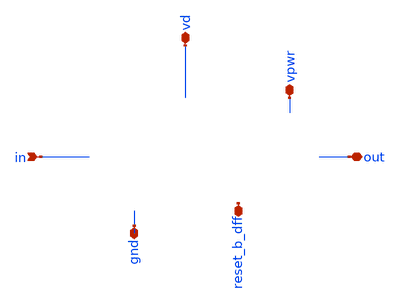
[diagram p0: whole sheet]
** sch_path: mag/sigma-delta_modulator/xschem/sigma-delta-pex.sch
* Copyright 2020 Stefan Frederik Schippers
* Licensed under the Apache License, Version 2.0 (the "License");
* you may not use this file except in compliance with the License.
* You may obtain a copy of the License at
* https://www.apache.org/licenses/LICENSE-2.0
* Unless required by applicable law or agreed to in writing, software
* distributed under the License is distributed on an "AS IS" BASIS,
* WITHOUT WARRANTIES OR CONDITIONS OF ANY KIND, either express or implied.
* See the License for the specific language governing permissions and
* limitations under the License.
**.subckt sigma-delta-pex in gnd out reset_b_dff vpwr vd
*.ipin in
*.iopin gnd
*.iopin out
*.iopin reset_b_dff
*.iopin vpwr
*.iopin vd
**** begin user architecture code



* NGSPICE file created from sigma-delta.ext - technology: sky130A

*.subckt sigma-delta reset_b_dff gnd vd in clk vpwr out
X0 a_n1599_309# a_n1774_335# a_n1420_335# gnd.t20 sky130_fd_pr__nfet_01v8 ad=0.109 pd=1.36 as=0.064
+ ps=0.725 w=0.42 l=0.15
X1 a_n2266_4800# a_n2100_3468# gnd.t7 sky130_fd_pr__res_xhigh_po_0p35 l=4.5
X2 a_n1124_4800# a_n958_3468# gnd.t50 sky130_fd_pr__res_xhigh_po_0p35 l=4.5
X3 x1.Q a_n1599_309# vpwr.t5 vpwr.t4 sky130_fd_pr__pfet_01v8_hvt ad=0.28 pd=2.56 as=0.213 ps=1.67
+ w=1 l=0.15
X4 a_n2339_335# a_n2689_335# a_n2434_335# vpwr.t15 sky130_fd_pr__pfet_01v8_hvt ad=0.0724 pd=0.765
+ as=0.0651 ps=0.73 w=0.42 l=0.15
X5 a_n2121_577# a_n2339_335# vpwr.t21 vpwr.t20 sky130_fd_pr__pfet_01v8_hvt ad=0.129 pd=1.18 as=0.218
+ ps=2.2 w=0.84 l=0.15
X6 a_n1420_335# reset_b_dff.t0 gnd.t52 gnd.t51 sky130_fd_pr__nfet_01v8 ad=0.064 pd=0.725 as=0.125
+ ps=1.01 w=0.42 l=0.15
X7 a_n792_4800# a_n626_3468# gnd.t8 sky130_fd_pr__res_xhigh_po_0p35 l=4.5
X8 a_n2714_2632# a_n2880_1800# gnd.t10 sky130_fd_pr__res_xhigh_po_0p35 l=2
X9 out.t0 a_n1035_335# gnd.t19 gnd.t18 sky130_fd_pr__nfet_01v8 ad=0.169 pd=1.82 as=0.1 ps=0.985
+ w=0.65 l=0.15
X10 a_n1934_4800# a_n2100_3468# gnd.t27 sky130_fd_pr__res_xhigh_po_0p35 l=4.5
X11 in_comp a_n1884_1800# gnd.t26 sky130_fd_pr__res_xhigh_po_0p35 l=2
X12 a_n1612_701# a_n2689_335# a_n1774_335# vpwr.t14 sky130_fd_pr__pfet_01v8_hvt ad=0.0567 pd=0.69
+ as=0.0588 ps=0.7 w=0.42 l=0.15
X13 a_n2077_335# a_n2121_577# a_n2243_335# gnd.t41 sky130_fd_pr__nfet_01v8 ad=0.0441 pd=0.63 as=0.14
+ ps=1.1 w=0.42 l=0.15
X14 a_n2434_335# x1.D gnd.t44 gnd.t43 sky130_fd_pr__nfet_01v8 ad=0.066 pd=0.745 as=0.221 ps=1.89
+ w=0.42 l=0.15
X15 a_n1599_309# reset_b_dff.t1 vpwr.t11 vpwr.t10 sky130_fd_pr__pfet_01v8_hvt ad=0.0567 pd=0.69
+ as=0.0819 ps=0.81 w=0.42 l=0.15
X16 a_n2598_4800# a_n2764_3468# gnd.t25 sky130_fd_pr__res_xhigh_po_0p35 l=4.5
X17 a_n1665_335# a_n2855_335# a_n1774_335# gnd.t38 sky130_fd_pr__nfet_01v8 ad=0.0669 pd=0.75
+ as=0.0711 ps=0.755 w=0.36 l=0.15
X18 a_n1456_4800# in_int gnd.t32 sky130_fd_pr__res_xhigh_po_0p35 l=4.5
X19 gnd.t6 a_n1599_309# a_n1665_335# gnd.t5 sky130_fd_pr__nfet_01v8 ad=0.125 pd=1.01 as=0.0669
+ ps=0.75 w=0.42 l=0.15
X20 a_n2434_335# x1.D vpwr.t25 vpwr.t24 sky130_fd_pr__pfet_01v8_hvt ad=0.0651 pd=0.73 as=0.109
+ ps=1.36 w=0.42 l=0.15
X21 vpwr.t3 a_n1599_309# a_n1612_701# vpwr.t2 sky130_fd_pr__pfet_01v8_hvt ad=0.0819 pd=0.81
+ as=0.0567 ps=0.69 w=0.42 l=0.15
X22 vpwr.t9 a_n1774_335# a_n1599_309# vpwr.t8 sky130_fd_pr__pfet_01v8_hvt ad=0.213 pd=1.67 as=0.0567
+ ps=0.69 w=0.42 l=0.15
X23 a_n2121_577# a_n2339_335# gnd.t40 gnd.t39 sky130_fd_pr__nfet_01v8 ad=0.0999 pd=0.985 as=0.135
+ ps=1.15 w=0.64 l=0.15
X24 vpwr.t27 clk.t0 a_n2855_335# vpwr.t26 sky130_fd_pr__pfet_01v8_hvt ad=0.0864 pd=0.91 as=0.166
+ ps=1.8 w=0.64 l=0.15
X25 gnd.t15 reset_b_dff.t2 a_n2077_335# gnd.t14 sky130_fd_pr__nfet_01v8 ad=0.135 pd=1.15 as=0.0441
+ ps=0.63 w=0.42 l=0.15
X26 vpwr.t1 a_n1599_309# a_n1035_335# vpwr.t0 sky130_fd_pr__pfet_01v8_hvt ad=0.154 pd=1.34 as=0.166
+ ps=1.8 w=0.64 l=0.15
X27 gnd.t4 a_n1599_309# a_n1035_335# gnd.t3 sky130_fd_pr__nfet_01v8 ad=0.1 pd=0.985 as=0.109 ps=1.36
+ w=0.42 l=0.15
X28 a_n2266_4800# a_n2432_3468# gnd.t17 sky130_fd_pr__res_xhigh_po_0p35 l=4.5
X29 a_n2050_2632# a_n2216_1800# gnd.t11 sky130_fd_pr__res_xhigh_po_0p35 l=2
X30 gnd.t22 clk.t1 a_n2855_335# gnd.t21 sky130_fd_pr__nfet_01v8 ad=0.0567 pd=0.69 as=0.109 ps=1.36
+ w=0.42 l=0.15
X31 a_n2243_335# a_n2689_335# a_n2339_335# gnd.t34 sky130_fd_pr__nfet_01v8 ad=0.14 pd=1.1 as=0.0594
+ ps=0.69 w=0.36 l=0.15
X32 vd.t1 in_comp x1.D vd.t0 sky130_fd_pr__pfet_01v8 ad=0.87 pd=6.58 as=0.87 ps=6.58 w=3 l=0.15
X33 a_n1124_4800# a_n1290_3468# gnd.t45 sky130_fd_pr__res_xhigh_po_0p35 l=4.5
X34 a_n2339_335# a_n2855_335# a_n2434_335# gnd.t37 sky130_fd_pr__nfet_01v8 ad=0.0594 pd=0.69
+ as=0.066 ps=0.745 w=0.36 l=0.15
X35 a_n460_4800# x1.Q gnd.t53 sky130_fd_pr__res_xhigh_po_0p35 l=4.5
X36 a_n2689_335# a_n2855_335# vpwr.t19 vpwr.t18 sky130_fd_pr__pfet_01v8_hvt ad=0.166 pd=1.8
+ as=0.0864 ps=0.91 w=0.64 l=0.15
X37 a_n2231_701# a_n2855_335# a_n2339_335# vpwr.t17 sky130_fd_pr__pfet_01v8_hvt ad=0.116 pd=0.97
+ as=0.0724 ps=0.765 w=0.42 l=0.15
X38 a_n2689_335# a_n2855_335# gnd.t36 gnd.t35 sky130_fd_pr__nfet_01v8 ad=0.109 pd=1.36 as=0.0567
+ ps=0.69 w=0.42 l=0.15
X39 a_n1774_335# a_n2855_335# a_n2121_577# vpwr.t16 sky130_fd_pr__pfet_01v8_hvt ad=0.0588 pd=0.7
+ as=0.129 ps=1.18 w=0.42 l=0.15
X40 a_n2382_2632# a_n2548_1800# gnd.t31 sky130_fd_pr__res_xhigh_po_0p35 l=2
X41 in_int a_n2880_1800# gnd.t16 sky130_fd_pr__res_xhigh_po_0p35 l=2
X42 x1.Q a_n1599_309# gnd.t2 gnd.t1 sky130_fd_pr__nfet_01v8 ad=0.169 pd=1.82 as=0.169 ps=1.82 w=0.65
+ l=0.15
X43 in_comp gnd.t30 sky130_fd_pr__cap_mim_m3_1 l=27.2 w=27.2
X44 a_n460_4800# a_n626_3468# gnd.t13 sky130_fd_pr__res_xhigh_po_0p35 l=4.5
X45 a_n2231_701# reset_b_dff.t3 vpwr.t13 vpwr.t12 sky130_fd_pr__pfet_01v8_hvt ad=0.109 pd=1.36
+ as=0.0703 ps=0.755 w=0.42 l=0.15
X46 a_n2930_4800# a_n2764_3468# gnd.t12 sky130_fd_pr__res_xhigh_po_0p35 l=4.5
X47 in_int gnd.t42 sky130_fd_pr__cap_mim_m3_1 l=27.2 w=27.2
X48 a_n2714_2632# a_n2548_1800# gnd.t24 sky130_fd_pr__res_xhigh_po_0p35 l=2
X49 gnd.t29 in_comp x1.D gnd.t28 sky130_fd_pr__nfet_01v8 ad=0.29 pd=2.58 as=0.29 ps=2.58 w=1 l=0.15
X50 a_n1934_4800# in_int gnd.t46 sky130_fd_pr__res_xhigh_po_0p35 l=4.5
X51 a_n792_4800# a_n958_3468# gnd.t9 sky130_fd_pr__res_xhigh_po_0p35 l=4.5
X52 vpwr.t23 a_n2121_577# a_n2231_701# vpwr.t22 sky130_fd_pr__pfet_01v8_hvt ad=0.0703 pd=0.755
+ as=0.116 ps=0.97 w=0.42 l=0.15
X53 a_n1774_335# a_n2689_335# a_n2121_577# gnd.t33 sky130_fd_pr__nfet_01v8 ad=0.0711 pd=0.755
+ as=0.0999 ps=0.985 w=0.36 l=0.15
X54 a_n2598_4800# a_n2432_3468# gnd.t49 sky130_fd_pr__res_xhigh_po_0p35 l=4.5
X55 a_n2382_2632# a_n2216_1800# gnd.t48 sky130_fd_pr__res_xhigh_po_0p35 l=2
X56 a_n2930_4800# in.t0 gnd.t23 sky130_fd_pr__res_xhigh_po_0p35 l=4.5
X57 a_n1456_4800# a_n1290_3468# gnd.t0 sky130_fd_pr__res_xhigh_po_0p35 l=4.5
X58 a_n2050_2632# a_n1884_1800# gnd.t47 sky130_fd_pr__res_xhigh_po_0p35 l=2
X59 out.t1 a_n1035_335# vpwr.t7 vpwr.t6 sky130_fd_pr__pfet_01v8_hvt ad=0.26 pd=2.52 as=0.154 ps=1.34
+ w=1 l=0.15
R0 gnd.n76 gnd.n12 1509.66
R1 gnd.n9 gnd.n3 1273.6
R2 gnd.n10 gnd.n9 1263.33
R3 gnd.t18 gnd.n84 1127.78
R4 gnd.t35 gnd.t43 1049.58
R5 gnd.n84 gnd.n83 788.875
R6 gnd.t1 gnd.t3 773.808
R7 gnd.t20 gnd.t1 773.808
R8 gnd.t34 gnd.t41 683.255
R9 gnd.t5 gnd.t51 613.284
R10 gnd.t14 gnd.t39 543.312
R11 gnd.t33 gnd.t38 448.644
R12 gnd.t39 gnd.t33 407.485
R13 gnd.t3 gnd.t18 399.252
R14 gnd.t38 gnd.t5 395.137
R15 gnd.t37 gnd.t34 395.137
R16 gnd.t43 gnd.t37 391.021
R17 gnd.t51 gnd.t20 374.557
R18 gnd.t21 gnd.t35 345.745
R19 gnd.t41 gnd.t14 296.353
R20 gnd gnd.t21 267.541
R21 gnd.n12 gnd.t53 238.407
R22 gnd.n23 gnd.t44 215.036
R23 gnd.n2 gnd.t23 190.731
R24 gnd.t53 gnd.t13 184.073
R25 gnd.t13 gnd.t8 184.073
R26 gnd.t8 gnd.t9 184.073
R27 gnd.t9 gnd.t50 184.073
R28 gnd.t50 gnd.t45 184.073
R29 gnd.t45 gnd.t0 184.073
R30 gnd.n7 gnd.t26 176.31
R31 gnd.n32 gnd.t2 154.317
R32 gnd.n81 gnd.n1 149.835
R33 gnd.n81 gnd.n80 149.835
R34 gnd.n34 gnd.n33 128.757
R35 gnd.t27 gnd.t11 128.63
R36 gnd.t7 gnd.t48 128.63
R37 gnd.t17 gnd.t31 128.63
R38 gnd.t49 gnd.t24 128.63
R39 gnd.t25 gnd.t10 128.63
R40 gnd.t12 gnd.t16 128.63
R41 gnd.n30 gnd.n29 116.754
R42 gnd.n7 gnd.t32 114.215
R43 gnd.n62 gnd.n21 107.24
R44 gnd.n49 gnd.n48 107.24
R45 gnd.n29 gnd.t52 100.001
R46 gnd.t46 gnd.n4 99.7989
R47 gnd.n80 gnd.n78 98.6358
R48 gnd.n48 gnd.t15 72.8576
R49 gnd.n29 gnd.t6 70.0005
R50 gnd.n48 gnd.t40 60.5809
R51 gnd.n33 gnd.t4 57.1434
R52 gnd.t26 gnd.t46 55.444
R53 gnd.t47 gnd.t27 55.444
R54 gnd.t11 gnd.t7 55.444
R55 gnd.t48 gnd.t17 55.444
R56 gnd.t31 gnd.t49 55.444
R57 gnd.t24 gnd.t25 55.444
R58 gnd.t10 gnd.t12 55.444
R59 gnd.n21 gnd.t36 38.5719
R60 gnd.n21 gnd.t22 38.5719
R61 gnd.n37 gnd.n36 34.6358
R62 gnd.n38 gnd.n37 34.6358
R63 gnd.n42 gnd.n41 34.6358
R64 gnd.n43 gnd.n42 34.6358
R65 gnd.n43 gnd.n27 34.6358
R66 gnd.n47 gnd.n27 34.6358
R67 gnd.n51 gnd.n50 34.6358
R68 gnd.n51 gnd.n25 34.6358
R69 gnd.n55 gnd.n25 34.6358
R70 gnd.n56 gnd.n55 34.6358
R71 gnd.n57 gnd.n56 34.6358
R72 gnd.n61 gnd.n23 29.7417
R73 gnd.n4 gnd.t47 28.8311
R74 gnd.n36 gnd.n32 27.8593
R75 gnd.n12 gnd.n11 26.7279
R76 gnd.n33 gnd.t19 25.4291
R77 gnd.n63 gnd.n62 24.4919
R78 gnd.n62 gnd.n61 22.9652
R79 gnd.n38 gnd.n30 17.6946
R80 gnd.n16 gnd.t29 17.405
R81 gnd.n57 gnd.n23 14.6829
R82 gnd.n34 gnd.n32 10.9075
R83 gnd.n16 gnd.n15 9.33321
R84 gnd.n50 gnd.n49 7.90638
R85 gnd.n50 gnd.n26 4.6505
R86 gnd.n59 gnd.n23 4.6505
R87 gnd.n62 gnd.n22 4.6505
R88 gnd.n52 gnd.n51 4.6505
R89 gnd.n53 gnd.n25 4.6505
R90 gnd.n55 gnd.n54 4.6505
R91 gnd.n56 gnd.n24 4.6505
R92 gnd.n58 gnd.n57 4.6505
R93 gnd.n61 gnd.n60 4.6505
R94 gnd.n36 gnd.n35 4.6505
R95 gnd.n37 gnd.n31 4.6505
R96 gnd.n39 gnd.n38 4.6505
R97 gnd.n41 gnd.n40 4.6505
R98 gnd.n42 gnd.n28 4.6505
R99 gnd.n44 gnd.n43 4.6505
R100 gnd.n45 gnd.n27 4.6505
R101 gnd.n47 gnd.n46 4.6505
R102 gnd.n65 gnd.n20 4.5005
R103 gnd.n65 gnd.n64 4.5005
R104 gnd.n41 gnd.n30 2.63579
R105 gnd.n65 gnd.n19 2.25328
R106 gnd.n49 gnd.n47 1.88285
R107 gnd gnd.n66 1.72422
R108 gnd.n68 gnd 1.25931
R109 gnd.n69 gnd.n68 0.575502
R110 gnd.n78 gnd.n77 0.541165
R111 gnd.n77 gnd.n76 0.541165
R112 gnd.n75 gnd.n74 0.347269
R113 gnd.n76 gnd.n75 0.347269
R114 gnd.n67 gnd.t30 0.258247
R115 gnd.n35 gnd.n34 0.144332
R116 gnd.n35 gnd.n31 0.120292
R117 gnd.n39 gnd.n31 0.120292
R118 gnd.n40 gnd.n39 0.120292
R119 gnd.n40 gnd.n28 0.120292
R120 gnd.n44 gnd.n28 0.120292
R121 gnd.n45 gnd.n44 0.120292
R122 gnd.n46 gnd.n45 0.120292
R123 gnd.n46 gnd.n26 0.120292
R124 gnd.n52 gnd.n26 0.120292
R125 gnd.n53 gnd.n52 0.120292
R126 gnd.n54 gnd.n53 0.120292
R127 gnd.n54 gnd.n24 0.120292
R128 gnd.n58 gnd.n24 0.120292
R129 gnd.n59 gnd.n58 0.120292
R130 gnd.n60 gnd.n59 0.120292
R131 gnd.n60 gnd.n22 0.120292
R132 gnd.n1 gnd.n0 0.10956
R133 gnd.n0 gnd.t28 0.10956
R134 gnd.n80 gnd.n79 0.10956
R135 gnd.n68 gnd.n67 0.103314
R136 gnd.n73 gnd.n14 0.084913
R137 gnd.n14 gnd.n13 0.0845034
R138 gnd.n22 gnd.n20 0.0734167
R139 gnd.n82 gnd.n81 0.0425017
R140 gnd.n83 gnd.n82 0.0425017
R141 gnd.n64 gnd 0.0330521
R142 gnd.n20 gnd.n18 0.0265417
R143 gnd.n67 gnd.t42 0.0261457
R144 gnd gnd.n63 0.0226354
R145 gnd.n19 gnd.n18 0.0114272
R146 gnd.n63 gnd.n19 0.0113582
R147 gnd.n66 gnd.n65 0.0110001
R148 gnd.n70 gnd.n16 0.00867757
R149 gnd.n70 gnd.n69 0.00634112
R150 gnd.n64 gnd 0.00570833
R151 gnd.n9 gnd.n8 0.00517349
R152 gnd.n8 gnd.n7 0.00517349
R153 gnd.n6 gnd.n5 0.00517349
R154 gnd.n7 gnd.n6 0.00517349
R155 gnd.n73 gnd.n72 0.00440917
R156 gnd.n3 gnd.n2 0.0043402
R157 gnd.n11 gnd.n10 0.0043402
R158 gnd.n72 gnd.n71 0.00391284
R159 gnd.n71 gnd.n70 0.00391159
R160 gnd.n66 gnd.n18 0.00100955
R161 gnd.n76 gnd.n73 0.00100353
R162 gnd.n69 gnd.n17 0.00051897
R163 vpwr.t18 vpwr.t24 790.188
R164 vpwr.t4 vpwr.t0 648.131
R165 vpwr.t12 vpwr.t20 583.023
R166 vpwr.n45 vpwr 548.548
R167 vpwr.n26 vpwr.t21 514.011
R168 vpwr.t8 vpwr.t4 485.358
R169 vpwr.t17 vpwr.t22 414.33
R170 vpwr.n2 vpwr.t25 375.277
R171 vpwr.t2 vpwr.t10 319.627
R172 vpwr.n20 vpwr.n9 311.957
R173 vpwr.n42 vpwr.n1 311.894
R174 vpwr.n29 vpwr.n28 309.18
R175 vpwr.t20 vpwr.t16 292.991
R176 vpwr.t15 vpwr.t17 292.991
R177 vpwr.n13 vpwr.n10 292.5
R178 vpwr.n15 vpwr.n14 292.5
R179 vpwr.t0 vpwr.t6 287.072
R180 vpwr.t22 vpwr.t12 287.072
R181 vpwr.t24 vpwr.t15 272.274
R182 vpwr.t16 vpwr.t14 254.518
R183 vpwr.t10 vpwr.t8 248.599
R184 vpwr.t14 vpwr.t2 248.599
R185 vpwr.t26 vpwr.t18 244.306
R186 vpwr vpwr.t26 186.556
R187 vpwr.n14 vpwr.n13 182.929
R188 vpwr.n12 vpwr.n11 148.689
R189 vpwr.n9 vpwr.t3 119.608
R190 vpwr.n28 vpwr.t23 93.81
R191 vpwr.n13 vpwr.t9 68.0124
R192 vpwr.n28 vpwr.t13 63.3219
R193 vpwr.n9 vpwr.t11 63.3219
R194 vpwr.n11 vpwr.t1 61.9158
R195 vpwr.n1 vpwr.t19 41.5552
R196 vpwr.n1 vpwr.t27 41.5552
R197 vpwr.n41 vpwr.n40 34.6358
R198 vpwr.n34 vpwr.n4 34.6358
R199 vpwr.n35 vpwr.n34 34.6358
R200 vpwr.n36 vpwr.n35 34.6358
R201 vpwr.n30 vpwr.n27 34.6358
R202 vpwr.n21 vpwr.n7 34.6358
R203 vpwr.n25 vpwr.n7 34.6358
R204 vpwr.n36 vpwr.n2 32.377
R205 vpwr.n26 vpwr.n25 32.0005
R206 vpwr.n11 vpwr.t7 30.239
R207 vpwr.n20 vpwr.n19 30.1181
R208 vpwr.n14 vpwr.t5 29.316
R209 vpwr.n42 vpwr.n41 22.9652
R210 vpwr.n21 vpwr.n20 20.3299
R211 vpwr.n40 vpwr.n2 18.0711
R212 vpwr.n15 vpwr.n12 13.9946
R213 vpwr.n19 vpwr.n10 12.8758
R214 vpwr.n27 vpwr.n26 9.41227
R215 vpwr.n29 vpwr.n4 6.02403
R216 vpwr.n16 vpwr.n15 5.00414
R217 vpwr.n20 vpwr.n8 4.6505
R218 vpwr.n26 vpwr.n6 4.6505
R219 vpwr.n38 vpwr.n2 4.6505
R220 vpwr.n17 vpwr.n16 4.6505
R221 vpwr.n19 vpwr.n18 4.6505
R222 vpwr.n22 vpwr.n21 4.6505
R223 vpwr.n23 vpwr.n7 4.6505
R224 vpwr.n25 vpwr.n24 4.6505
R225 vpwr.n27 vpwr.n5 4.6505
R226 vpwr.n31 vpwr.n30 4.6505
R227 vpwr.n32 vpwr.n4 4.6505
R228 vpwr.n34 vpwr.n33 4.6505
R229 vpwr.n35 vpwr.n3 4.6505
R230 vpwr.n37 vpwr.n36 4.6505
R231 vpwr.n40 vpwr.n39 4.6505
R232 vpwr.n41 vpwr.n0 4.6505
R233 vpwr.n16 vpwr.n10 4.07323
R234 vpwr.n43 vpwr.n42 3.93272
R235 vpwr.n30 vpwr.n29 3.76521
R236 vpwr vpwr.n51 0.223
R237 vpwr.n17 vpwr.n12 0.144332
R238 vpwr.n43 vpwr.n0 0.138831
R239 vpwr.n18 vpwr.n17 0.120292
R240 vpwr.n18 vpwr.n8 0.120292
R241 vpwr.n22 vpwr.n8 0.120292
R242 vpwr.n23 vpwr.n22 0.120292
R243 vpwr.n24 vpwr.n23 0.120292
R244 vpwr.n24 vpwr.n6 0.120292
R245 vpwr.n6 vpwr.n5 0.120292
R246 vpwr.n31 vpwr.n5 0.120292
R247 vpwr.n32 vpwr.n31 0.120292
R248 vpwr.n33 vpwr.n32 0.120292
R249 vpwr.n33 vpwr.n3 0.120292
R250 vpwr.n37 vpwr.n3 0.120292
R251 vpwr.n38 vpwr.n37 0.120292
R252 vpwr.n39 vpwr.n38 0.120292
R253 vpwr.n39 vpwr.n0 0.120292
R254 vpwr.n44 vpwr.n43 0.107496
R255 vpwr.n47 vpwr 0.088
R256 vpwr.n51 vpwr.n50 0.0197304
R257 vpwr.n44 vpwr 0.0174271
R258 vpwr vpwr.n44 0.01675
R259 vpwr.n48 vpwr.n47 0.013
R260 vpwr.n50 vpwr.n49 0.00412567
R261 vpwr.n49 vpwr.n48 0.003625
R262 vpwr.n50 vpwr.n45 0.0015496
R263 vpwr.n49 vpwr.n46 0.000543305
R264 reset_b_dff.n14 reset_b_dff.t3 413.313
R265 reset_b_dff.n7 reset_b_dff.t1 344.005
R266 reset_b_dff.n6 reset_b_dff.t0 187.321
R267 reset_b_dff.n7 reset_b_dff.n5 152
R268 reset_b_dff.n14 reset_b_dff.t2 126.127
R269 reset_b_dff.n6 reset_b_dff.n1 73.2067
R270 reset_b_dff reset_b_dff.n4 14.0185
R271 reset_b_dff.n11 reset_b_dff.n10 9.3005
R272 reset_b_dff.n8 reset_b_dff.n2 9.3005
R273 reset_b_dff.n8 reset_b_dff.n7 9.3005
R274 reset_b_dff.n7 reset_b_dff.n6 9.15991
R275 reset_b_dff.n15 reset_b_dff.n14 7.02742
R276 reset_b_dff.n4 reset_b_dff 4.7293
R277 reset_b_dff.n9 reset_b_dff.n0 4.6505
R278 reset_b_dff.n18 reset_b_dff.n17 4.6505
R279 reset_b_dff.n4 reset_b_dff 4.53383
R280 reset_b_dff.n5 reset_b_dff 3.11401
R281 reset_b_dff.n17 reset_b_dff.n15 3.0725
R282 reset_b_dff.n24 reset_b_dff 2.98033
R283 reset_b_dff.n12 reset_b_dff 2.36657
R284 reset_b_dff.n5 reset_b_dff.n1 1.55726
R285 reset_b_dff.n10 reset_b_dff.n9 1.55726
R286 reset_b_dff.n8 reset_b_dff.n1 1.38428
R287 reset_b_dff.n9 reset_b_dff.n8 1.38428
R288 reset_b_dff.n10 reset_b_dff 1.38428
R289 reset_b_dff.n17 reset_b_dff.n16 1.2805
R290 reset_b_dff.n12 reset_b_dff 0.580857
R291 reset_b_dff.n3 reset_b_dff 0.196446
R292 reset_b_dff.n20 reset_b_dff 0.171696
R293 reset_b_dff.n20 reset_b_dff.n19 0.0901739
R294 reset_b_dff.n21 reset_b_dff.n20 0.0500874
R295 reset_b_dff.n13 reset_b_dff.n12 0.0466957
R296 reset_b_dff.n26 reset_b_dff.n25 0.0435328
R297 reset_b_dff.n18 reset_b_dff.n13 0.0331087
R298 reset_b_dff.n3 reset_b_dff.n2 0.02675
R299 reset_b_dff reset_b_dff.n11 0.0255
R300 reset_b_dff.n22 reset_b_dff.n21 0.0213989
R301 reset_b_dff.n24 reset_b_dff.n23 0.018111
R302 reset_b_dff.n19 reset_b_dff.n18 0.014087
R303 reset_b_dff.n25 reset_b_dff.n22 0.0127951
R304 reset_b_dff.n11 reset_b_dff.n0 0.01175
R305 reset_b_dff.n2 reset_b_dff.n0 0.0105
R306 reset_b_dff reset_b_dff.n3 0.00725676
R307 reset_b_dff reset_b_dff.n26 0.00459836
R308 reset_b_dff.n25 reset_b_dff.n24 0.0016109
R309 out.n0 out.t1 250.94
R310 out out.t0 144.601
R311 out.n0 out 4.7225
R312 out out.n0 3.35288
R313 clk.n3 clk.t0 294.557
R314 clk.n3 clk.t1 211.01
R315 clk.n4 clk.n3 8.28655
R316 clk.n2 clk 7.73487
R317 clk.n4 clk.n2 1.82961
R318 clk clk.n5 0.981259
R319 clk.n5 clk.n4 0.848973
R320 clk.n0 clk 0.385917
R321 clk.n1 clk.n0 0.03175
R322 clk.n2 clk.n1 0.00111796
R323 vd.n10 vd.n7 135.465
R324 vd.n13 vd.n12 101.647
R325 vd.n26 vd.t1 9.52337
R326 vd vd.n35 4.20467
R327 vd.n14 vd.n13 0.130052
R328 vd.n15 vd.n14 0.130052
R329 vd.n5 vd.n4 0.107375
R330 vd.n15 vd.n5 0.107375
R331 vd.n31 vd.n29 0.0456031
R332 vd.n25 vd.n23 0.0456031
R333 vd.n23 vd.n21 0.0456031
R334 vd.n34 vd.n33 0.0391598
R335 vd.n33 vd.n31 0.0391598
R336 vd.n12 vd.n11 0.0349892
R337 vd.n11 vd.t0 0.0349892
R338 vd.n9 vd.n8 0.0349892
R339 vd.n10 vd.n9 0.0333079
R340 vd.n26 vd.n25 0.0217629
R341 vd.n29 vd.n27 0.0198299
R342 vd.n16 vd.n3 0.0125538
R343 vd.n3 vd.n2 0.0120596
R344 vd.n7 vd.n6 0.00627981
R345 vd.n27 vd.n26 0.00501031
R346 vd.t0 vd.n10 0.00318081
R347 vd.n17 vd.n16 0.0018171
R348 vd.n18 vd.n17 0.00131751
R349 vd.n27 vd.n18 0.00131744
R350 vd.n33 vd.n32 0.00119114
R351 vd.n34 vd.n0 0.00101609
R352 vd.n16 vd.n15 0.00100038
R353 vd.n21 vd.n20 0.00100009
R354 vd.n29 vd.n28 0.000659706
R355 vd.n23 vd.n22 0.000659706
R356 vd.n31 vd.n1 0.000543686
R357 vd.n25 vd.n19 0.000543686
R358 vd.n35 vd.n34 0.000507883
R359 vd.n25 vd.n24 0.000507883
R360 vd.n31 vd.n30 0.000507883
R361 in in.t0 9.56433
C0 in_int vd 0.347f
C1 a_n2855_335# a_n1774_335# 0.102f
C2 x1.Q a_n2077_335# 9.75e-20
C3 x1.D reset_b_dff 0.223f
C4 x1.D clk 0.0102f
C5 x1.Q a_n2121_577# 0.00111f
C6 in_int a_n2930_4800# 0.00283f
C7 a_n2548_1800# in_comp 2.76e-19
C8 vpwr a_n2689_335# 0.57f
C9 vd x1.D 0.908f
C10 a_n2548_1800# in_int 0.00497f
C11 a_n1774_335# a_n2121_577# 0.0512f
C12 a_n2434_335# x1.D 0.164f
C13 a_n1035_335# a_n2689_335# 2.01e-19
C14 x1.Q a_n1884_1800# 0.00101f
C15 in_comp a_n2855_335# 2.02e-20
C16 a_n626_3468# a_n460_4800# 0.00434f
C17 a_n2216_1800# x1.Q 4.28e-19
C18 a_n2432_3468# a_n2764_3468# 0.296f
C19 a_n2548_1800# x1.D 3.98e-19
C20 a_n626_3468# vd 0.0129f
C21 a_n1420_335# reset_b_dff 0.00312f
C22 in_int a_n792_4800# 0.00627f
C23 a_n1420_335# clk 6.32e-21
C24 a_n2050_2632# a_n1884_1800# 0.00938f
C25 a_n2432_3468# in 4.07e-20
C26 a_n958_3468# x1.Q 5e-20
C27 a_n2050_2632# a_n2216_1800# 0.00938f
C28 x1.Q vpwr 0.175f
C29 a_n2339_335# out 7.05e-19
C30 a_n1599_309# reset_b_dff 0.28f
C31 a_n1599_309# clk 2.68e-20
C32 a_n2100_3468# x1.Q 1.43e-21
C33 a_n2855_335# x1.D 0.195f
C34 in_comp a_n2121_577# 7.49e-21
C35 x1.Q a_n1035_335# 0.226f
C36 vd a_n1599_309# 0.00172f
C37 vpwr a_n1774_335# 0.284f
C38 a_n2100_3468# a_n2050_2632# 0.00472f
C39 a_n2880_1800# clk 1.96e-19
C40 a_n1035_335# a_n1774_335# 7.05e-19
C41 a_n1612_701# a_n2121_577# 2.6e-19
C42 a_n2243_335# a_n2689_335# 2.28e-19
C43 a_n2077_335# x1.D 5.41e-20
C44 a_n2231_701# a_n2339_335# 0.0572f
C45 out reset_b_dff 0.00564f
C46 in_comp a_n1884_1800# 0.0188f
C47 out clk 4.76e-19
C48 a_n2382_2632# x1.Q 1.13e-19
C49 a_n2216_1800# in_comp 4.76e-19
C50 in_int a_n1884_1800# 0.00497f
C51 a_n2121_577# x1.D 6.24e-19
C52 a_n1124_4800# vd 0.00116f
C53 a_n1290_3468# vd 0.00171f
C54 in_int a_n2216_1800# 0.00497f
C55 a_n626_3468# a_n792_4800# 0.00473f
C56 vd out 0.0503f
C57 a_n958_3468# in_comp 7.16e-19
C58 a_n2382_2632# a_n2050_2632# 0.296f
C59 a_n2548_1800# a_n2714_2632# 0.00938f
C60 in_comp vpwr 0.00229f
C61 in_int a_n958_3468# 0.0502f
C62 a_n2231_701# reset_b_dff 0.013f
C63 in_int vpwr 0.00475f
C64 in_comp a_n1035_335# 0.00219f
C65 a_n2855_335# a_n1599_309# 0.0436f
C66 x1.Q a_n2243_335# 1.45e-19
C67 a_n2100_3468# in_int 0.339f
C68 a_n2880_1800# a_n2548_1800# 0.296f
C69 in_int a_n1035_335# 0.00192f
C70 a_n2548_1800# out 0.0144f
C71 vpwr a_n1612_701# 7.36e-19
C72 a_n2764_3468# a_n2930_4800# 0.00458f
C73 x1.Q a_n2689_335# 0.00137f
C74 a_n2930_4800# in 0.0056f
C75 vpwr x1.D 0.238f
C76 a_n2382_2632# in_comp 2.91e-19
C77 a_n1934_4800# vd 6.34e-20
C78 in_int a_n2598_4800# 0.00321f
C79 a_n2880_1800# a_n2855_335# 1.68e-19
C80 a_n1124_4800# a_n792_4800# 0.307f
C81 a_n2855_335# out 0.00153f
C82 a_n2382_2632# in_int 0.0611f
C83 a_n1035_335# x1.D 0.00209f
C84 a_n1774_335# a_n2689_335# 0.125f
C85 a_n626_3468# a_n958_3468# 0.303f
C86 a_n1665_335# reset_b_dff 7.93e-19
C87 a_n1665_335# clk 1.1e-20
C88 a_n2855_335# a_n2231_701# 9.73e-19
C89 a_n2339_335# reset_b_dff 0.165f
C90 a_n2121_577# out 3.73e-19
C91 a_n2339_335# clk 3.26e-19
C92 a_n2100_3468# a_n2266_4800# 0.00473f
C93 in_comp a_n2689_335# 1.41e-20
C94 x1.Q a_n1774_335# 0.00593f
C95 a_n2050_2632# x1.Q 2.81e-19
C96 vpwr a_n1599_309# 0.408f
C97 a_n1884_1800# out 0.0144f
C98 a_n2598_4800# a_n2266_4800# 0.303f
C99 a_n2243_335# x1.D 8.22e-19
C100 a_n1612_701# a_n2689_335# 1.46e-19
C101 a_n2216_1800# out 0.0144f
C102 a_n1035_335# a_n1599_309# 0.107f
C103 a_n2231_701# a_n2121_577# 0.0977f
C104 a_n2434_335# a_n2339_335# 0.0498f
C105 reset_b_dff clk 0.0302f
C106 a_n1124_4800# a_n958_3468# 0.00509f
C107 a_n1290_3468# a_n958_3468# 0.312f
C108 a_n2689_335# x1.D 0.229f
C109 a_n1456_4800# in_int 0.00837f
C110 vpwr out 0.584f
C111 vd reset_b_dff 2.96e-19
C112 in_comp x1.Q 0.425f
C113 in_int x1.Q 0.417f
C114 a_n2855_335# a_n1665_335# 2.56e-19
C115 a_n460_4800# vd 0.133f
C116 a_n2434_335# reset_b_dff 0.00224f
C117 a_n1035_335# out 0.0691f
C118 a_n2434_335# clk 3.09e-19
C119 a_n2382_2632# a_n2714_2632# 0.296f
C120 a_n2050_2632# in_comp 0.297f
C121 a_n2855_335# a_n2339_335# 0.115f
C122 in_comp a_n1774_335# 5.26e-20
C123 x1.Q a_n1612_701# 4.53e-20
C124 a_n2100_3468# in 1.53e-20
C125 in_int a_n2050_2632# 0.059f
C126 vpwr a_n2231_701# 0.143f
C127 x1.Q x1.D 0.0672f
C128 a_n2382_2632# out 0.00336f
C129 a_n2764_3468# a_n2598_4800# 0.00434f
C130 a_n1612_701# a_n1774_335# 0.00645f
C131 a_n2077_335# a_n2339_335# 0.00171f
C132 a_n1665_335# a_n2121_577# 4.2e-19
C133 a_n2855_335# reset_b_dff 0.312f
C134 a_n2855_335# clk 0.273f
C135 a_n1599_309# a_n2689_335# 0.0426f
C136 a_n1774_335# x1.D 9.45e-19
C137 a_n2339_335# a_n2121_577# 0.21f
C138 a_n2100_3468# a_n1934_4800# 0.00434f
C139 a_n626_3468# x1.Q 0.414f
C140 in_int in_comp 0.698f
C141 a_n792_4800# a_n460_4800# 0.299f
C142 a_n2855_335# vd 1.72e-20
C143 a_n2077_335# reset_b_dff 0.00407f
C144 a_n2077_335# clk 1.82e-20
C145 a_n1884_1800# a_n2339_335# 1.87e-19
C146 a_n792_4800# vd 0.00299f
C147 a_n2855_335# a_n2434_335# 0.0931f
C148 x1.Q a_n1420_335# 6.05e-19
C149 a_n2121_577# reset_b_dff 0.172f
C150 a_n2100_3468# a_n2432_3468# 0.302f
C151 a_n2689_335# out 0.0011f
C152 a_n2121_577# clk 1.78e-19
C153 in_comp x1.D 0.304f
C154 x1.Q a_n1599_309# 0.142f
C155 a_n2548_1800# a_n2855_335# 2.33e-20
C156 in_int x1.D 0.0174f
C157 vpwr a_n2339_335# 0.197f
C158 a_n1124_4800# a_n1456_4800# 0.3f
C159 a_n2432_3468# a_n2598_4800# 0.00482f
C160 a_n1456_4800# a_n1290_3468# 0.00473f
C161 a_n2432_3468# a_n2382_2632# 0.00472f
C162 a_n2216_1800# reset_b_dff 2.29e-19
C163 a_n2231_701# a_n2689_335# 0.0346f
C164 a_n1612_701# x1.D 2.11e-20
C165 a_n1774_335# a_n1599_309# 0.251f
C166 a_n1290_3468# x1.Q 1.87e-20
C167 a_n1884_1800# vd 1.16e-19
C168 x1.Q out 0.669f
C169 a_n626_3468# in_int 0.0192f
C170 vpwr reset_b_dff 0.205f
C171 vpwr clk 0.19f
C172 in_int a_n2266_4800# 0.00277f
C173 a_n1774_335# out 6.85e-19
C174 a_n1035_335# reset_b_dff 0.00144f
C175 a_n2050_2632# out 0.00336f
C176 a_n958_3468# vd 0.00352f
C177 vd vpwr 0.00696f
C178 a_n2855_335# a_n2121_577# 0.0701f
C179 in_comp a_n1599_309# 0.00158f
C180 x1.Q a_n2231_701# 3.66e-19
C181 a_n1456_4800# a_n1934_4800# 0.144f
C182 a_n2548_1800# a_n2216_1800# 0.296f
C183 in_int a_n1599_309# 0.00144f
C184 vd a_n1035_335# 0.00317f
C185 vpwr a_n2434_335# 0.0827f
C186 a_n2714_2632# in_comp 1.21e-19
C187 in_int a_n2714_2632# 0.399f
C188 a_n2077_335# a_n2121_577# 3.69e-19
C189 a_n2243_335# a_n2339_335# 0.0138f
C190 a_n1420_335# x1.D 4.54e-20
C191 a_n1665_335# a_n2689_335# 2.36e-20
C192 a_n1884_1800# a_n2855_335# 1.47e-19
C193 in_comp out 0.0553f
C194 a_n1124_4800# in_int 0.00679f
C195 a_n2339_335# a_n2689_335# 0.23f
C196 a_n1599_309# x1.D 0.004f
C197 a_n2880_1800# in_int 0.0164f
C198 a_n1290_3468# in_int 0.357f
C199 in_int out 0.00921f
C200 a_n2764_3468# in_int 0.0408f
C201 a_n2598_4800# a_n2930_4800# 0.296f
C202 a_n2855_335# vpwr 0.441f
C203 a_n792_4800# a_n958_3468# 0.00482f
C204 a_n2243_335# reset_b_dff 0.00292f
C205 a_n2243_335# clk 5.33e-20
C206 in_int in 0.0139f
C207 a_n2855_335# a_n1035_335# 4.71e-20
C208 a_n2216_1800# a_n2121_577# 1.53e-19
C209 x1.Q a_n1665_335# 1.47e-19
C210 a_n2382_2632# a_n2548_1800# 0.00938f
C211 out x1.D 0.294f
C212 a_n2689_335# reset_b_dff 0.0304f
C213 a_n2689_335# clk 0.00241f
C214 x1.Q a_n2339_335# 8.11e-19
C215 vd a_n2689_335# 1.08e-19
C216 a_n1420_335# a_n1599_309# 0.0074f
C217 a_n1665_335# a_n1774_335# 0.00742f
C218 a_n2243_335# a_n2434_335# 4.61e-19
C219 vpwr a_n2121_577# 0.205f
C220 a_n1934_4800# in_int 0.00787f
C221 a_n2216_1800# a_n1884_1800# 0.296f
C222 a_n2434_335# a_n2689_335# 0.0642f
C223 a_n1774_335# a_n2339_335# 7.99e-20
C224 a_n2231_701# x1.D 5.56e-20
C225 x1.Q reset_b_dff 0.0107f
C226 a_n1456_4800# vd 5.85e-19
C227 a_n2548_1800# a_n2689_335# 1.47e-19
C228 a_n2432_3468# in_int 0.0411f
C229 a_n460_4800# x1.Q 0.00839f
C230 a_n2855_335# a_n2243_335# 0.00134f
C231 x1.Q vd 0.186f
C232 a_n1774_335# reset_b_dff 0.239f
C233 a_n1599_309# out 0.00735f
C234 a_n1774_335# clk 6.46e-20
C235 a_n2880_1800# a_n2714_2632# 0.00938f
C236 in_comp a_n2339_335# 2.02e-20
C237 a_n2855_335# a_n2689_335# 0.906f
C238 a_n2714_2632# out 0.00336f
C239 x1.Q a_n2434_335# 7.58e-20
C240 vd a_n1774_335# 3.52e-19
C241 vpwr a_n1035_335# 0.198f
C242 a_n2764_3468# a_n2714_2632# 0.00472f
C243 a_n1124_4800# a_n1290_3468# 0.00536f
C244 a_n2382_2632# a_n2216_1800# 0.00938f
C245 a_n1934_4800# a_n2266_4800# 0.296f
C246 a_n2880_1800# out 0.0144f
C247 a_n1665_335# x1.D 2.42e-20
C248 a_n2243_335# a_n2121_577# 3.16e-19
C249 in_comp reset_b_dff 4.91e-20
C250 a_n2339_335# x1.D 0.00353f
C251 a_n2121_577# a_n2689_335# 0.186f
C252 a_n1290_3468# in 9.87e-22
C253 x1.Q a_n2855_335# 9.54e-19
C254 a_n2432_3468# a_n2266_4800# 0.00473f
C255 a_n792_4800# x1.Q 0.0032f
C256 in_int a_n460_4800# 0.0115f
C257 in_comp vd 0.833f
C258 a_n2764_3468# in 0.303f
C259 a_n1612_701# reset_b_dff 2.06e-19
C260 a_n1884_1800# a_n2689_335# 1.07e-19
C261 out gnd 1.09f
C262 reset_b_dff gnd 1.4f
C263 clk gnd 0.346f
C264 in gnd 0.529f
C265 vd gnd 4.19f
C266 vpwr gnd 2.89f
C267 a_n1420_335# gnd 0.00223f
C268 a_n1665_335# gnd 9.68e-19
C269 a_n2077_335# gnd 0.00579f
C270 a_n2243_335# gnd 0.00863f
C271 a_n2231_701# gnd 0.00469f
C272 a_n2434_335# gnd 0.08f
C273 a_n1035_335# gnd 0.213f
C274 a_n1774_335# gnd 0.275f
C275 a_n1599_309# gnd 0.741f
C276 a_n2339_335# gnd 0.281f
C277 a_n2121_577# gnd 0.194f
C278 a_n2689_335# gnd 0.332f
C279 x1.D gnd 2.59f
C280 a_n2855_335# gnd 0.701f
C281 in_comp gnd 75.8f
C282 a_n1884_1800# gnd 0.549f
C283 a_n2050_2632# gnd 0.331f
C284 a_n2216_1800# gnd 0.349f
C285 a_n2382_2632# gnd 0.331f
C286 a_n2548_1800# gnd 0.349f
C287 a_n2714_2632# gnd 0.331f
C288 a_n2880_1800# gnd 0.53f
C289 x1.Q gnd 1.42f
C290 a_n460_4800# gnd 0.523f
C291 a_n626_3468# gnd 0.353f
C292 a_n792_4800# gnd 0.385f
C293 a_n958_3468# gnd 0.359f
C294 a_n1124_4800# gnd 0.389f
C295 a_n1290_3468# gnd 0.364f
C296 a_n1456_4800# gnd 0.444f
C297 in_int gnd 69.9f
C298 a_n1934_4800# gnd 0.442f
C299 a_n2100_3468# gnd 0.351f
C300 a_n2266_4800# gnd 0.38f
C301 a_n2432_3468# gnd 0.35f
C302 a_n2598_4800# gnd 0.383f
C303 a_n2764_3468# gnd 0.35f
C304 a_n2930_4800# gnd 0.586f
*.ends





.include /foss/pdks/sky130A/libs.ref/sky130_fd_sc_hd/spice/sky130_fd_sc_hd.spice


**** end user architecture code
**.ends
.end
